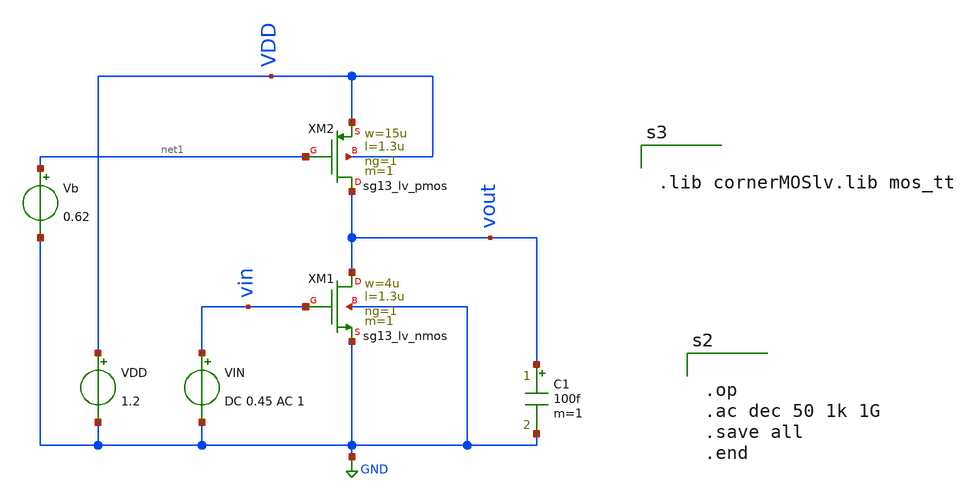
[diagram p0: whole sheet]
** sch_path: BTDay3-Ex/CS_Amplifier_Current.sch
**.subckt CS_Amplifier_Current
XXM1 vout vin GND GND sg13_lv_nmos w=4u l=1.3u ng=1 m=1 mm_ok=1
XXM2 vout net1 VDD VDD sg13_lv_pmos w=15u l=1.3u ng=1 m=1 mm_ok=1
VDD VDD GND 1.2
Vb net1 GND 0.62
VIN vin GND DC 0.45 AC 1
C1 vout GND 100f m=1
**** begin user architecture code


.op
.ac dec 50 1k 1G
.save all
.end




.lib cornerMOSlv.lib mos_tt


**** end user architecture code
**.ends
.GLOBAL GND
.end
